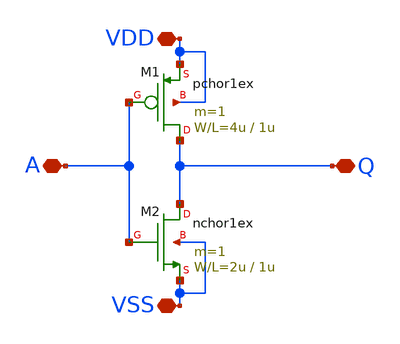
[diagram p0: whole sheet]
** sch_path: member_project/dokunira/inverter_layout/inv.sch
**.subckt inv A VDD VSS Q
*.iopin A
*.iopin VDD
*.iopin VSS
*.iopin Q
M1 Q A VDD VDD pchor1ex L=1u W=4u m=1
M2 Q A VSS VSS nchor1ex L=1u W=2u m=1
**.ends
.end
